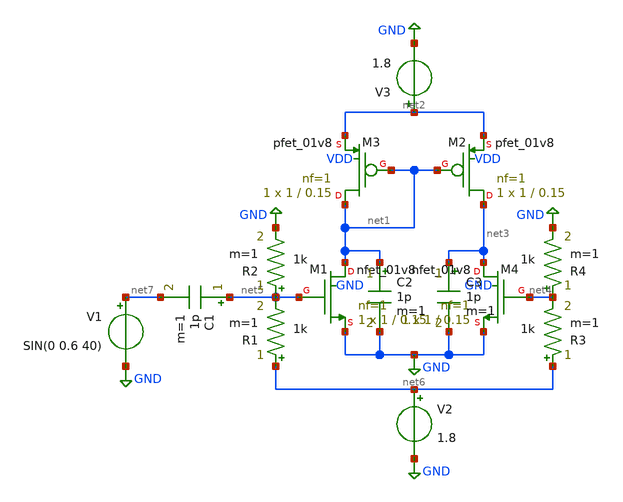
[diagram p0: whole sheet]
** sch_path: xschem/power-detector.sch
**.subckt power-detector
XM1 net1 net5 GND GND sky130_fd_pr__nfet_01v8 L=0.15 W=1 nf=1 ad='int((nf+1)/2) * W/nf * 0.29' as='int((nf+2)/2) * W/nf * 0.29'
+ pd='2*int((nf+1)/2) * (W/nf + 0.29)' ps='2*int((nf+2)/2) * (W/nf + 0.29)' nrd='0.29 / W' nrs='0.29 / W'
+ sa=0 sb=0 sd=0 mult=1 m=1
XM2 net3 net1 net2 VDD sky130_fd_pr__pfet_01v8 L=0.15 W=1 nf=1 ad='int((nf+1)/2) * W/nf * 0.29' as='int((nf+2)/2) * W/nf * 0.29'
+ pd='2*int((nf+1)/2) * (W/nf + 0.29)' ps='2*int((nf+2)/2) * (W/nf + 0.29)' nrd='0.29 / W' nrs='0.29 / W'
+ sa=0 sb=0 sd=0 mult=1 m=1
XM3 net1 net1 net2 VDD sky130_fd_pr__pfet_01v8 L=0.15 W=1 nf=1 ad='int((nf+1)/2) * W/nf * 0.29' as='int((nf+2)/2) * W/nf * 0.29'
+ pd='2*int((nf+1)/2) * (W/nf + 0.29)' ps='2*int((nf+2)/2) * (W/nf + 0.29)' nrd='0.29 / W' nrs='0.29 / W'
+ sa=0 sb=0 sd=0 mult=1 m=1
XM4 net3 net4 GND GND sky130_fd_pr__nfet_01v8 L=0.15 W=1 nf=1 ad='int((nf+1)/2) * W/nf * 0.29' as='int((nf+2)/2) * W/nf * 0.29'
+ pd='2*int((nf+1)/2) * (W/nf + 0.29)' ps='2*int((nf+2)/2) * (W/nf + 0.29)' nrd='0.29 / W' nrs='0.29 / W'
+ sa=0 sb=0 sd=0 mult=1 m=1
R1 net6 net5 1k m=1
R2 net5 GND 1k m=1
R3 net6 net4 1k m=1
R4 net4 GND 1k m=1
C1 net5 net7 1p m=1
C2 net1 GND 1p m=1
C3 net3 GND 1p m=1
V1 net7 GND SIN(0 0.6 40)
V2 net6 GND 1.8
V3 net2 GND 1.8
**** begin user architecture code
 ** manual skywater pdks install (with patches applied)
* .lib $::SKYWATER_MODELS/models/sky130.lib.spice tt

** opencircuitdesign pdks install
.lib $::SKYWATER_MODELS/sky130.lib.spice tt

.param mc_mm_switch=0
.param mc_pr_switch=0



.tran 0.001s 0.1s


**** end user architecture code
**.ends
.GLOBAL GND
.end
